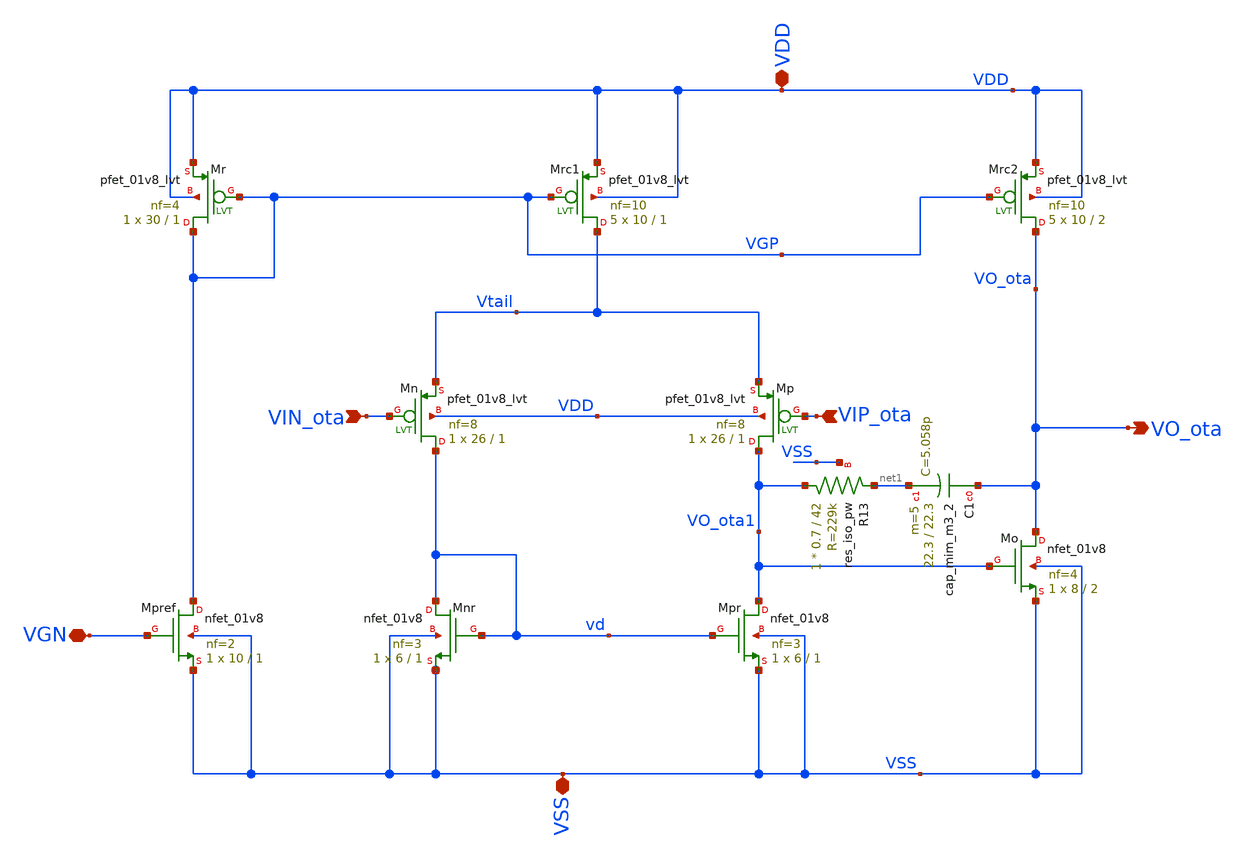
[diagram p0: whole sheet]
** sch_path: xschem/OTA.sch
**.subckt OTA VIN_ota VO_ota VSS VDD VIP_ota VGN
*.ipin VIN_ota
*.opin VO_ota
*.iopin VSS
*.iopin VDD
*.ipin VIP_ota
*.iopin VGN
XMpr VO_ota1 vd VSS VSS sky130_fd_pr__nfet_01v8 L=1 W=6 nf=3 ad='int((3 + 1)/2) * 6 / 3 * 0.29' as='int((3 + 2)/2) * 6 / 3 * 0.29'
+ pd='2*int((3 + 1)/2) * (6 / 3 + 0.29)' ps='2*int((3 + 2)/2) * (6 / 3 + 0.29)' nrd='0.29 / 6 ' nrs='0.29 / 6 '
+ sa=0 sb=0 sd=0 mult=1 m=1
XMnr vd vd VSS VSS sky130_fd_pr__nfet_01v8 L=1 W=6 nf=3 ad='int((3 + 1)/2) * 6 / 3 * 0.29' as='int((3 + 2)/2) * 6 / 3 * 0.29'
+ pd='2*int((3 + 1)/2) * (6 / 3 + 0.29)' ps='2*int((3 + 2)/2) * (6 / 3 + 0.29)' nrd='0.29 / 6 ' nrs='0.29 / 6 '
+ sa=0 sb=0 sd=0 mult=1 m=1
XMo VO_ota VO_ota1 VSS VSS sky130_fd_pr__nfet_01v8 L=2 W=8 nf=4 ad='int((4 + 1)/2) * 8 / 4 * 0.29' as='int((4 + 2)/2) * 8 / 4 * 0.29'
+ pd='2*int((4 + 1)/2) * (8 / 4 + 0.29)' ps='2*int((4 + 2)/2) * (8 / 4 + 0.29)' nrd='0.29 / 8 ' nrs='0.29 / 8 '
+ sa=0 sb=0 sd=0 mult=1 m=1
XMrc2 VO_ota VGP VDD VDD sky130_fd_pr__pfet_01v8_lvt L=2 W=10 nf=10 ad='int((10 + 1)/2) * 10 / 10 * 0.29'
+ as='int((10 + 2)/2) * 10 / 10 * 0.29' pd='2*int((10 + 1)/2) * (10 / 10 + 0.29)' ps='2*int((10 + 2)/2) * (10 / 10 + 0.29)'
+ nrd='0.29 / 10 ' nrs='0.29 / 10 ' sa=0 sb=0 sd=0 mult=5 m=5
XC1 VO_ota net1 sky130_fd_pr__cap_mim_m3_2 W=22.3 L=22.3 MF=5 m=5
XMp VO_ota1 VIP_ota Vtail VDD sky130_fd_pr__pfet_01v8_lvt L=1 W=26 nf=8 ad='int((8 + 1)/2) * 26 / 8 * 0.29'
+ as='int((8 + 2)/2) * 26 / 8 * 0.29' pd='2*int((8 + 1)/2) * (26 / 8 + 0.29)' ps='2*int((8 + 2)/2) * (26 / 8 + 0.29)'
+ nrd='0.29 / 26 ' nrs='0.29 / 26 ' sa=0 sb=0 sd=0 mult=1 m=1
XMn vd VIN_ota Vtail VDD sky130_fd_pr__pfet_01v8_lvt L=1 W=26 nf=8 ad='int((8 + 1)/2) * 26 / 8 * 0.29'
+ as='int((8 + 2)/2) * 26 / 8 * 0.29' pd='2*int((8 + 1)/2) * (26 / 8 + 0.29)' ps='2*int((8 + 2)/2) * (26 / 8 + 0.29)'
+ nrd='0.29 / 26 ' nrs='0.29 / 26 ' sa=0 sb=0 sd=0 mult=1 m=1
XMrc1 Vtail VGP VDD VDD sky130_fd_pr__pfet_01v8_lvt L=1 W=10 nf=10 ad='int((10 + 1)/2) * 10 / 10 * 0.29'
+ as='int((10 + 2)/2) * 10 / 10 * 0.29' pd='2*int((10 + 1)/2) * (10 / 10 + 0.29)' ps='2*int((10 + 2)/2) * (10 / 10 + 0.29)'
+ nrd='0.29 / 10 ' nrs='0.29 / 10 ' sa=0 sb=0 sd=0 mult=5 m=5
XR13 VO_ota1 net1 VSS sky130_fd_pr__res_iso_pw W=0.7 L=42 m=1
XMr VGP VGP VDD VDD sky130_fd_pr__pfet_01v8_lvt L=1 W=30 nf=4 ad='int((4 + 1)/2) * 30 / 4 * 0.29' as='int((4 + 2)/2) * 30 / 4 * 0.29'
+ pd='2*int((4 + 1)/2) * (30 / 4 + 0.29)' ps='2*int((4 + 2)/2) * (30 / 4 + 0.29)' nrd='0.29 / 30 ' nrs='0.29 / 30 '
+ sa=0 sb=0 sd=0 mult=1 m=1
XMpref VGP VGN VSS VSS sky130_fd_pr__nfet_01v8 L=1 W=10 nf=2 ad='int((2 + 1)/2) * 10 / 2 * 0.29' as='int((2 + 2)/2) * 10 / 2 * 0.29'
+ pd='2*int((2 + 1)/2) * (10 / 2 + 0.29)' ps='2*int((2 + 2)/2) * (10 / 2 + 0.29)' nrd='0.29 / 10 ' nrs='0.29 / 10 '
+ sa=0 sb=0 sd=0 mult=1 m=1
**.ends
.end
